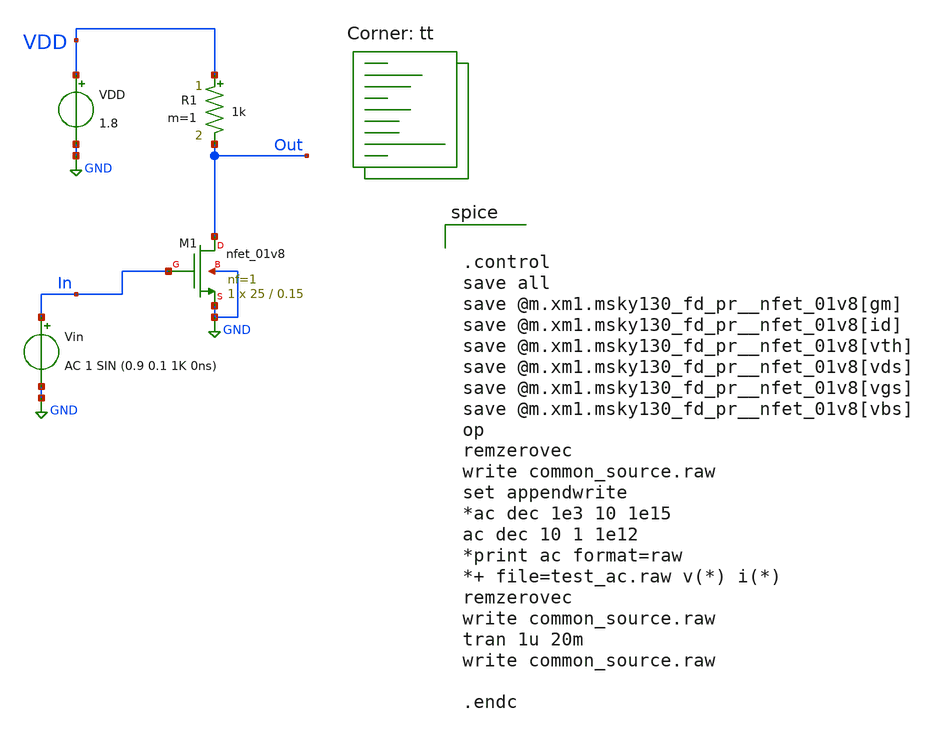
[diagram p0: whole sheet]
** sch_path: common_source.sch
**.subckt common_source
XM1 Out In GND GND sky130_fd_pr__nfet_01v8 L=0.15 W=25 nf=1 ad='int((nf+1)/2) * W/nf * 0.29' as='int((nf+2)/2) * W/nf * 0.29'
+ pd='2*int((nf+1)/2) * (W/nf + 0.29)' ps='2*int((nf+2)/2) * (W/nf + 0.29)' nrd='0.29 / W' nrs='0.29 / W'
+ sa=0 sb=0 sd=0 mult=1 m=1
R1 VDD Out 1k m=1
Vin In GND AC 1 SIN (0.9 0.1 1K 0ns)
VDD VDD GND 1.8
**** begin user architecture code
.lib $::SKYWATER_MODELS/sky130.lib.spice tt


.control
save all
save @m.xm1.msky130_fd_pr__nfet_01v8[gm]
save @m.xm1.msky130_fd_pr__nfet_01v8[id]
save @m.xm1.msky130_fd_pr__nfet_01v8[vth]
save @m.xm1.msky130_fd_pr__nfet_01v8[vds]
save @m.xm1.msky130_fd_pr__nfet_01v8[vgs]
save @m.xm1.msky130_fd_pr__nfet_01v8[vbs]
op
remzerovec
write common_source.raw
set appendwrite
*ac dec 1e3 10 1e15
ac dec 10 1 1e12
*print ac format=raw
*+ file=test_ac.raw v(*) i(*)
remzerovec
write common_source.raw
tran 1u 20m
write common_source.raw

.endc


**** end user architecture code
**.ends
.GLOBAL GND
.end
